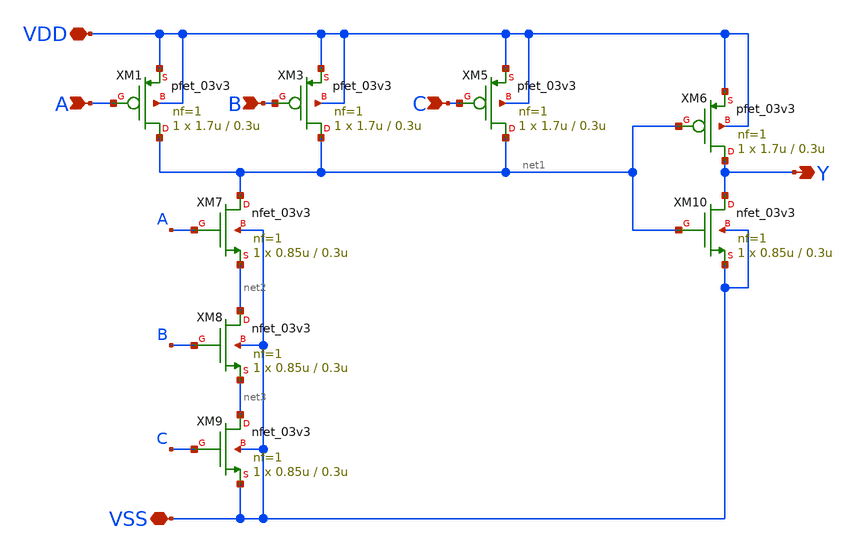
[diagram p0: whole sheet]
** sch_path: gf180mcu_osu_sc_gp12t3v3/xschem/gf180mcu_osu_sc_gp12t3v3__and3_1.sch
**.subckt gf180mcu_osu_sc_gp12t3v3__and3_1 A B Y C VDD VSS
*.ipin A
*.ipin B
*.opin Y
*.ipin C
*.iopin VDD
*.iopin VSS
XM1 net1 A VDD VDD pfet_03v3 L=0.3u W=1.7u nf=1 ad='int((nf+1)/2) * W/nf * 0.18u' as='int((nf+2)/2) * W/nf * 0.18u'
+ pd='2*int((nf+1)/2) * (W/nf + 0.18u)' ps='2*int((nf+2)/2) * (W/nf + 0.18u)' nrd='0.18u / W' nrs='0.18u / W'
+ sa=0 sb=0 sd=0 m=1
XM3 net1 B VDD VDD pfet_03v3 L=0.3u W=1.7u nf=1 ad='int((nf+1)/2) * W/nf * 0.18u' as='int((nf+2)/2) * W/nf * 0.18u'
+ pd='2*int((nf+1)/2) * (W/nf + 0.18u)' ps='2*int((nf+2)/2) * (W/nf + 0.18u)' nrd='0.18u / W' nrs='0.18u / W'
+ sa=0 sb=0 sd=0 m=1
XM5 net1 C VDD VDD pfet_03v3 L=0.3u W=1.7u nf=1 ad='int((nf+1)/2) * W/nf * 0.18u' as='int((nf+2)/2) * W/nf * 0.18u'
+ pd='2*int((nf+1)/2) * (W/nf + 0.18u)' ps='2*int((nf+2)/2) * (W/nf + 0.18u)' nrd='0.18u / W' nrs='0.18u / W'
+ sa=0 sb=0 sd=0 m=1
XM6 Y net1 VDD VDD pfet_03v3 L=0.3u W=1.7u nf=1 ad='int((nf+1)/2) * W/nf * 0.18u' as='int((nf+2)/2) * W/nf * 0.18u'
+ pd='2*int((nf+1)/2) * (W/nf + 0.18u)' ps='2*int((nf+2)/2) * (W/nf + 0.18u)' nrd='0.18u / W' nrs='0.18u / W'
+ sa=0 sb=0 sd=0 m=1
XM7 net1 A net2 VSS nfet_03v3 L=0.3u W=0.85u nf=1 ad='int((nf+1)/2) * W/nf * 0.18u' as='int((nf+2)/2) * W/nf * 0.18u'
+ pd='2*int((nf+1)/2) * (W/nf + 0.18u)' ps='2*int((nf+2)/2) * (W/nf + 0.18u)' nrd='0.18u / W' nrs='0.18u / W'
+ sa=0 sb=0 sd=0 m=1
XM8 net2 B net3 VSS nfet_03v3 L=0.3u W=0.85u nf=1 ad='int((nf+1)/2) * W/nf * 0.18u' as='int((nf+2)/2) * W/nf * 0.18u'
+ pd='2*int((nf+1)/2) * (W/nf + 0.18u)' ps='2*int((nf+2)/2) * (W/nf + 0.18u)' nrd='0.18u / W' nrs='0.18u / W'
+ sa=0 sb=0 sd=0 m=1
XM9 net3 C VSS VSS nfet_03v3 L=0.3u W=0.85u nf=1 ad='int((nf+1)/2) * W/nf * 0.18u' as='int((nf+2)/2) * W/nf * 0.18u'
+ pd='2*int((nf+1)/2) * (W/nf + 0.18u)' ps='2*int((nf+2)/2) * (W/nf + 0.18u)' nrd='0.18u / W' nrs='0.18u / W'
+ sa=0 sb=0 sd=0 m=1
XM10 Y net1 VSS VSS nfet_03v3 L=0.3u W=0.85u nf=1 ad='int((nf+1)/2) * W/nf * 0.18u' as='int((nf+2)/2) * W/nf * 0.18u'
+ pd='2*int((nf+1)/2) * (W/nf + 0.18u)' ps='2*int((nf+2)/2) * (W/nf + 0.18u)' nrd='0.18u / W' nrs='0.18u / W'
+ sa=0 sb=0 sd=0 m=1
**.ends
.end
